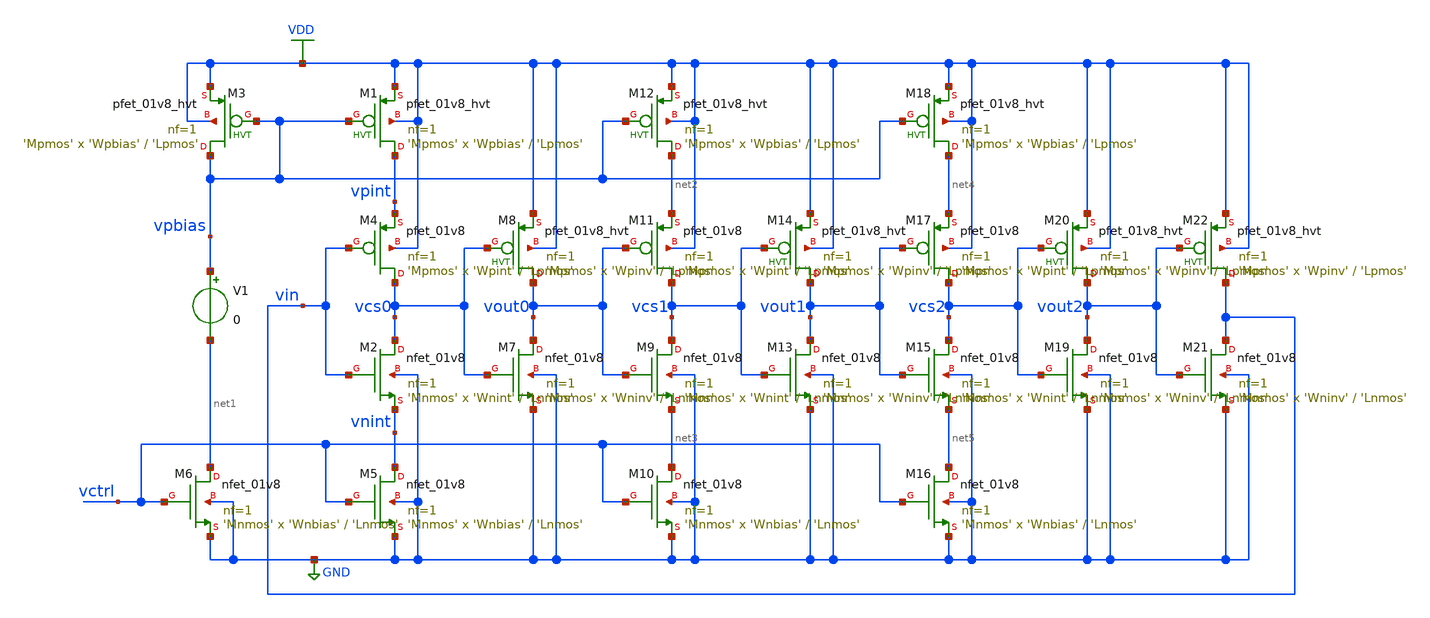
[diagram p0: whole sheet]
** sch_path: designs/cs_ring_osc.sch
* Copyright 2020 Stefan Frederik Schippers
* Licensed under the Apache License, Version 2.0 (the "License");
* you may not use this file except in compliance with the License.
* You may obtain a copy of the License at
* https://www.apache.org/licenses/LICENSE-2.0
* Unless required by applicable law or agreed to in writing, software
* distributed under the License is distributed on an "AS IS" BASIS,
* WITHOUT WARRANTIES OR CONDITIONS OF ANY KIND, either express or implied.
* See the License for the specific language governing permissions and
* limitations under the License.
**.subckt cs_ring_osc
V1 vpbias net1 0
XM6 net1 vctrl GND GND sky130_fd_pr__nfet_01v8 L='Lnmos' W='Wnbias' nf=1 ad='int((nf+1)/2) * W/nf * 0.29'
+ as='int((nf+2)/2) * W/nf * 0.29' pd='2*int((nf+1)/2) * (W/nf + 0.29)' ps='2*int((nf+2)/2) * (W/nf + 0.29)'
+ nrd='0.29 / W' nrs='0.29 / W' sa=0 sb=0 sd=0 mult='Mnmos' m='Mnmos'
XM2 vcs0 vin vnint GND sky130_fd_pr__nfet_01v8 L='Lnmos' W='Wnint' nf=1 ad='int((nf+1)/2) * W/nf * 0.29'
+ as='int((nf+2)/2) * W/nf * 0.29' pd='2*int((nf+1)/2) * (W/nf + 0.29)' ps='2*int((nf+2)/2) * (W/nf + 0.29)'
+ nrd='0.29 / W' nrs='0.29 / W' sa=0 sb=0 sd=0 mult='Mnmos' m='Mnmos'
XM5 vnint vctrl GND GND sky130_fd_pr__nfet_01v8 L='Lnmos' W='Wnbias' nf=1 ad='int((nf+1)/2) * W/nf * 0.29'
+ as='int((nf+2)/2) * W/nf * 0.29' pd='2*int((nf+1)/2) * (W/nf + 0.29)' ps='2*int((nf+2)/2) * (W/nf + 0.29)'
+ nrd='0.29 / W' nrs='0.29 / W' sa=0 sb=0 sd=0 mult='Mnmos' m='Mnmos'
XM4 vcs0 vin vpint VDD sky130_fd_pr__pfet_01v8 L='Lpmos' W='Wpint' nf=1 ad='int((nf+1)/2) * W/nf * 0.29'
+ as='int((nf+2)/2) * W/nf * 0.29' pd='2*int((nf+1)/2) * (W/nf + 0.29)' ps='2*int((nf+2)/2) * (W/nf + 0.29)'
+ nrd='0.29 / W' nrs='0.29 / W' sa=0 sb=0 sd=0 mult='Mpmos' m='Mpmos'
XM1 vpint vpbias VDD VDD sky130_fd_pr__pfet_01v8_hvt L='Lpmos' W='Wpbias' nf=1 ad='int((nf+1)/2) * W/nf * 0.29'
+ as='int((nf+2)/2) * W/nf * 0.29' pd='2*int((nf+1)/2) * (W/nf + 0.29)' ps='2*int((nf+2)/2) * (W/nf + 0.29)'
+ nrd='0.29 / W' nrs='0.29 / W' sa=0 sb=0 sd=0 mult='Mpmos' m='Mpmos'
XM3 vpbias vpbias VDD VDD sky130_fd_pr__pfet_01v8_hvt L='Lpmos' W='Wpbias' nf=1 ad='int((nf+1)/2) * W/nf * 0.29'
+ as='int((nf+2)/2) * W/nf * 0.29' pd='2*int((nf+1)/2) * (W/nf + 0.29)' ps='2*int((nf+2)/2) * (W/nf + 0.29)'
+ nrd='0.29 / W' nrs='0.29 / W' sa=0 sb=0 sd=0 mult='Mpmos' m='Mpmos'
XM7 vout0 vcs0 GND GND sky130_fd_pr__nfet_01v8 L='Lnmos' W='Wninv' nf=1 ad='int((nf+1)/2) * W/nf * 0.29'
+ as='int((nf+2)/2) * W/nf * 0.29' pd='2*int((nf+1)/2) * (W/nf + 0.29)' ps='2*int((nf+2)/2) * (W/nf + 0.29)'
+ nrd='0.29 / W' nrs='0.29 / W' sa=0 sb=0 sd=0 mult='Mnmos' m='Mnmos'
XM9 vcs1 vout0 net3 GND sky130_fd_pr__nfet_01v8 L='Lnmos' W='Wnint' nf=1 ad='int((nf+1)/2) * W/nf * 0.29'
+ as='int((nf+2)/2) * W/nf * 0.29' pd='2*int((nf+1)/2) * (W/nf + 0.29)' ps='2*int((nf+2)/2) * (W/nf + 0.29)'
+ nrd='0.29 / W' nrs='0.29 / W' sa=0 sb=0 sd=0 mult='Mnmos' m='Mnmos'
XM10 net3 vctrl GND GND sky130_fd_pr__nfet_01v8 L='Lnmos' W='Wnbias' nf=1 ad='int((nf+1)/2) * W/nf * 0.29'
+ as='int((nf+2)/2) * W/nf * 0.29' pd='2*int((nf+1)/2) * (W/nf + 0.29)' ps='2*int((nf+2)/2) * (W/nf + 0.29)'
+ nrd='0.29 / W' nrs='0.29 / W' sa=0 sb=0 sd=0 mult='Mnmos' m='Mnmos'
XM11 vcs1 vout0 net2 VDD sky130_fd_pr__pfet_01v8 L='Lpmos' W='Wpint' nf=1 ad='int((nf+1)/2) * W/nf * 0.29'
+ as='int((nf+2)/2) * W/nf * 0.29' pd='2*int((nf+1)/2) * (W/nf + 0.29)' ps='2*int((nf+2)/2) * (W/nf + 0.29)'
+ nrd='0.29 / W' nrs='0.29 / W' sa=0 sb=0 sd=0 mult='Mpmos' m='Mpmos'
XM12 net2 vpbias VDD VDD sky130_fd_pr__pfet_01v8_hvt L='Lpmos' W='Wpbias' nf=1 ad='int((nf+1)/2) * W/nf * 0.29'
+ as='int((nf+2)/2) * W/nf * 0.29' pd='2*int((nf+1)/2) * (W/nf + 0.29)' ps='2*int((nf+2)/2) * (W/nf + 0.29)'
+ nrd='0.29 / W' nrs='0.29 / W' sa=0 sb=0 sd=0 mult='Mpmos' m='Mpmos'
XM13 vout1 vcs1 GND GND sky130_fd_pr__nfet_01v8 L='Lnmos' W='Wninv' nf=1 ad='int((nf+1)/2) * W/nf * 0.29'
+ as='int((nf+2)/2) * W/nf * 0.29' pd='2*int((nf+1)/2) * (W/nf + 0.29)' ps='2*int((nf+2)/2) * (W/nf + 0.29)'
+ nrd='0.29 / W' nrs='0.29 / W' sa=0 sb=0 sd=0 mult='Mnmos' m='Mnmos'
XM8 vout0 vcs0 VDD VDD sky130_fd_pr__pfet_01v8_hvt L='Lpmos' W='Wpinv' nf=1 ad='int((nf+1)/2) * W/nf * 0.29'
+ as='int((nf+2)/2) * W/nf * 0.29' pd='2*int((nf+1)/2) * (W/nf + 0.29)' ps='2*int((nf+2)/2) * (W/nf + 0.29)'
+ nrd='0.29 / W' nrs='0.29 / W' sa=0 sb=0 sd=0 mult='Mpmos' m='Mpmos'
XM14 vout1 vcs1 VDD VDD sky130_fd_pr__pfet_01v8_hvt L='Lpmos' W='Wpinv' nf=1 ad='int((nf+1)/2) * W/nf * 0.29'
+ as='int((nf+2)/2) * W/nf * 0.29' pd='2*int((nf+1)/2) * (W/nf + 0.29)' ps='2*int((nf+2)/2) * (W/nf + 0.29)'
+ nrd='0.29 / W' nrs='0.29 / W' sa=0 sb=0 sd=0 mult='Mpmos' m='Mpmos'
XM15 vcs2 vout1 net5 GND sky130_fd_pr__nfet_01v8 L='Lnmos' W='Wnint' nf=1 ad='int((nf+1)/2) * W/nf * 0.29'
+ as='int((nf+2)/2) * W/nf * 0.29' pd='2*int((nf+1)/2) * (W/nf + 0.29)' ps='2*int((nf+2)/2) * (W/nf + 0.29)'
+ nrd='0.29 / W' nrs='0.29 / W' sa=0 sb=0 sd=0 mult='Mnmos' m='Mnmos'
XM16 net5 vctrl GND GND sky130_fd_pr__nfet_01v8 L='Lnmos' W='Wnbias' nf=1 ad='int((nf+1)/2) * W/nf * 0.29'
+ as='int((nf+2)/2) * W/nf * 0.29' pd='2*int((nf+1)/2) * (W/nf + 0.29)' ps='2*int((nf+2)/2) * (W/nf + 0.29)'
+ nrd='0.29 / W' nrs='0.29 / W' sa=0 sb=0 sd=0 mult='Mnmos' m='Mnmos'
XM17 vcs2 vout1 net4 VDD sky130_fd_pr__pfet_01v8 L='Lpmos' W='Wpint' nf=1 ad='int((nf+1)/2) * W/nf * 0.29'
+ as='int((nf+2)/2) * W/nf * 0.29' pd='2*int((nf+1)/2) * (W/nf + 0.29)' ps='2*int((nf+2)/2) * (W/nf + 0.29)'
+ nrd='0.29 / W' nrs='0.29 / W' sa=0 sb=0 sd=0 mult='Mpmos' m='Mpmos'
XM18 net4 vpbias VDD VDD sky130_fd_pr__pfet_01v8_hvt L='Lpmos' W='Wpbias' nf=1 ad='int((nf+1)/2) * W/nf * 0.29'
+ as='int((nf+2)/2) * W/nf * 0.29' pd='2*int((nf+1)/2) * (W/nf + 0.29)' ps='2*int((nf+2)/2) * (W/nf + 0.29)'
+ nrd='0.29 / W' nrs='0.29 / W' sa=0 sb=0 sd=0 mult='Mpmos' m='Mpmos'
XM19 vout2 vcs2 GND GND sky130_fd_pr__nfet_01v8 L='Lnmos' W='Wninv' nf=1 ad='int((nf+1)/2) * W/nf * 0.29'
+ as='int((nf+2)/2) * W/nf * 0.29' pd='2*int((nf+1)/2) * (W/nf + 0.29)' ps='2*int((nf+2)/2) * (W/nf + 0.29)'
+ nrd='0.29 / W' nrs='0.29 / W' sa=0 sb=0 sd=0 mult='Mnmos' m='Mnmos'
XM20 vout2 vcs2 VDD VDD sky130_fd_pr__pfet_01v8_hvt L='Lpmos' W='Wpinv' nf=1 ad='int((nf+1)/2) * W/nf * 0.29'
+ as='int((nf+2)/2) * W/nf * 0.29' pd='2*int((nf+1)/2) * (W/nf + 0.29)' ps='2*int((nf+2)/2) * (W/nf + 0.29)'
+ nrd='0.29 / W' nrs='0.29 / W' sa=0 sb=0 sd=0 mult='Mpmos' m='Mpmos'
XM21 vin vout2 GND GND sky130_fd_pr__nfet_01v8 L='Lnmos' W='Wninv' nf=1 ad='int((nf+1)/2) * W/nf * 0.29'
+ as='int((nf+2)/2) * W/nf * 0.29' pd='2*int((nf+1)/2) * (W/nf + 0.29)' ps='2*int((nf+2)/2) * (W/nf + 0.29)'
+ nrd='0.29 / W' nrs='0.29 / W' sa=0 sb=0 sd=0 mult='Mnmos' m='Mnmos'
XM22 vin vout2 VDD VDD sky130_fd_pr__pfet_01v8_hvt L='Lpmos' W='Wpinv' nf=1 ad='int((nf+1)/2) * W/nf * 0.29'
+ as='int((nf+2)/2) * W/nf * 0.29' pd='2*int((nf+1)/2) * (W/nf + 0.29)' ps='2*int((nf+2)/2) * (W/nf + 0.29)'
+ nrd='0.29 / W' nrs='0.29 / W' sa=0 sb=0 sd=0 mult='Mpmos' m='Mpmos'
**** begin user architecture code

.include $::SKYWATER_MODELS/cells/nfet_01v8/sky130_fd_pr__nfet_01v8__tt.corner.spice
.include $::SKYWATER_MODELS/cells/nfet_01v8_lvt/sky130_fd_pr__nfet_01v8_lvt__tt.corner.spice
.include $::SKYWATER_MODELS/cells/pfet_01v8/sky130_fd_pr__pfet_01v8__tt.corner.spice
.include $::SKYWATER_MODELS/cells/nfet_03v3_nvt/sky130_fd_pr__nfet_03v3_nvt__tt.corner.spice
.include $::SKYWATER_MODELS/cells/nfet_05v0_nvt/sky130_fd_pr__nfet_05v0_nvt__tt.corner.spice
.include $::SKYWATER_MODELS/cells/esd_nfet_01v8/sky130_fd_pr__esd_nfet_01v8__tt.corner.spice
.include $::SKYWATER_MODELS/cells/pfet_01v8_lvt/sky130_fd_pr__pfet_01v8_lvt__tt.corner.spice
.include $::SKYWATER_MODELS/cells/pfet_01v8_hvt/sky130_fd_pr__pfet_01v8_hvt__tt.corner.spice
.include $::SKYWATER_MODELS/cells/esd_pfet_g5v0d10v5/sky130_fd_pr__esd_pfet_g5v0d10v5__tt.corner.spice
.include $::SKYWATER_MODELS/cells/pfet_g5v0d10v5/sky130_fd_pr__pfet_g5v0d10v5__tt.corner.spice
.include $::SKYWATER_MODELS/cells/pfet_g5v0d16v0/sky130_fd_pr__pfet_g5v0d16v0__tt.corner.spice
.include $::SKYWATER_MODELS/cells/nfet_g5v0d10v5/sky130_fd_pr__nfet_g5v0d10v5__tt.corner.spice
.include $::SKYWATER_MODELS/cells/nfet_g5v0d16v0/sky130_fd_pr__nfet_g5v0d16v0__tt_discrete.corner.spice
.include $::SKYWATER_MODELS/cells/esd_nfet_g5v0d10v5/sky130_fd_pr__esd_nfet_g5v0d10v5__tt.corner.spice
.include $::SKYWATER_MODELS/models/corners/tt/nonfet.spice
* Mismatch parameters
.include $::SKYWATER_MODELS/cells/nfet_01v8/sky130_fd_pr__nfet_01v8__mismatch.corner.spice
.include $::SKYWATER_MODELS/cells/pfet_01v8/sky130_fd_pr__pfet_01v8__mismatch.corner.spice
.include $::SKYWATER_MODELS/cells/nfet_01v8_lvt/sky130_fd_pr__nfet_01v8_lvt__mismatch.corner.spice
.include $::SKYWATER_MODELS/cells/pfet_01v8_lvt/sky130_fd_pr__pfet_01v8_lvt__mismatch.corner.spice
.include $::SKYWATER_MODELS/cells/pfet_01v8_hvt/sky130_fd_pr__pfet_01v8_hvt__mismatch.corner.spice
.include $::SKYWATER_MODELS/cells/nfet_g5v0d10v5/sky130_fd_pr__nfet_g5v0d10v5__mismatch.corner.spice
.include $::SKYWATER_MODELS/cells/pfet_g5v0d10v5/sky130_fd_pr__pfet_g5v0d10v5__mismatch.corner.spice
.include $::SKYWATER_MODELS/cells/nfet_05v0_nvt/sky130_fd_pr__nfet_05v0_nvt__mismatch.corner.spice
.include $::SKYWATER_MODELS/cells/nfet_03v3_nvt/sky130_fd_pr__nfet_03v3_nvt__mismatch.corner.spice
* Resistor$::SKYWATER_MODELS/Capacitor
.include $::SKYWATER_MODELS/models/r+c/res_typical__cap_typical.spice
.include $::SKYWATER_MODELS/models/r+c/res_typical__cap_typical__lin.spice
* Special cells
.include $::SKYWATER_MODELS/models/corners/tt/specialized_cells.spice
* All models
.include $::SKYWATER_MODELS/models/all.spice
* Corner
.include $::SKYWATER_MODELS/models/corners/tt/rf.spice

**** end user architecture code
**.ends
.GLOBAL VDD
.GLOBAL GND
**** begin user architecture code

.include cs_ring_osc_commands.spice

**** end user architecture code
.end
